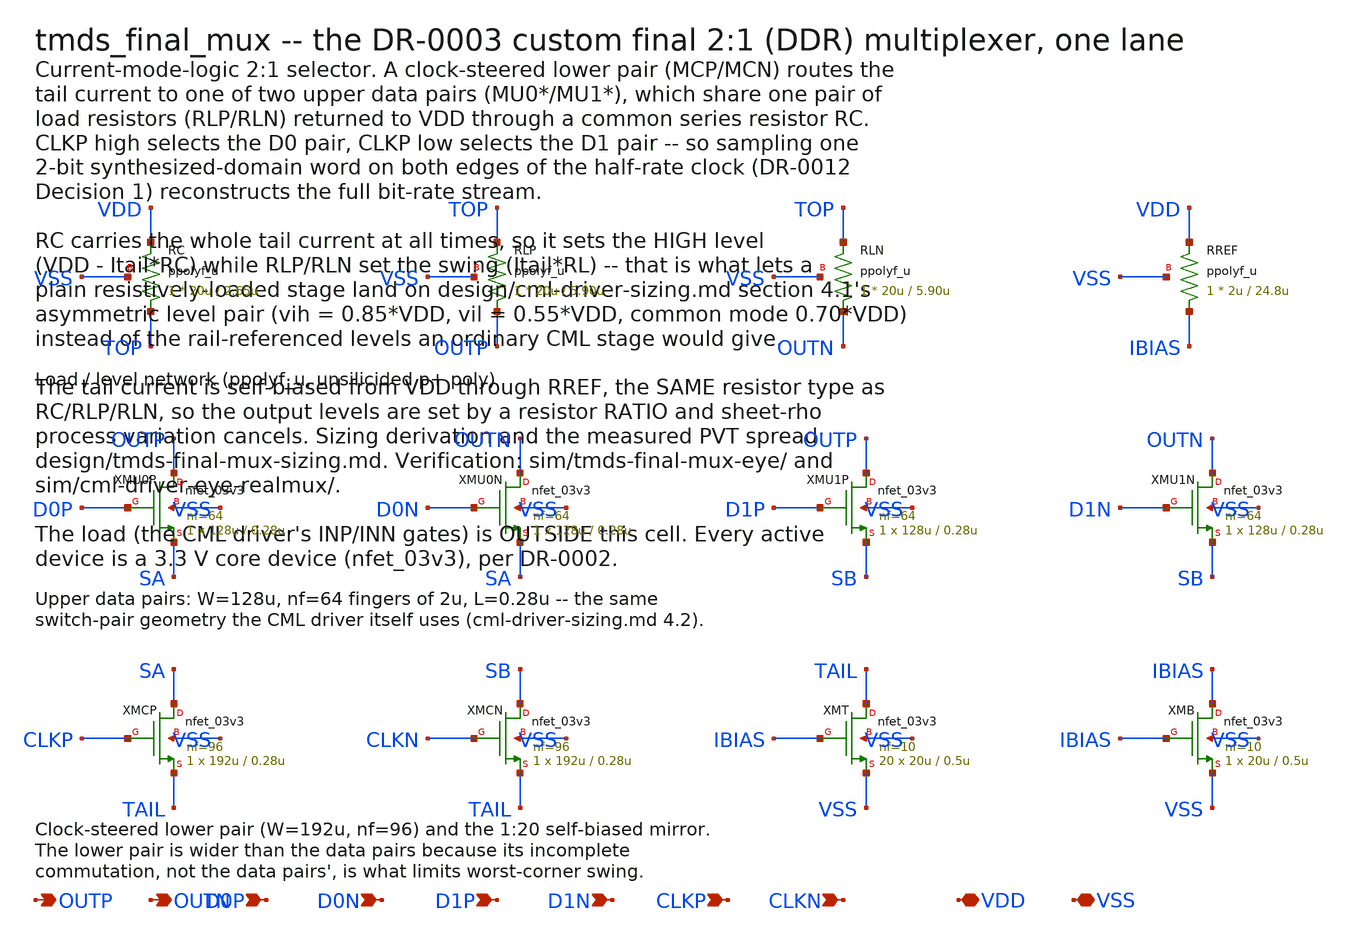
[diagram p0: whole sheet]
** sch_path: design/tmds_final_mux.sch
**.subckt tmds_final_mux OUTP OUTN D0P D0N D1P D1N CLKP CLKN VDD VSS
*.opin OUTP
*.opin OUTN
*.ipin D0P
*.ipin D0N
*.ipin D1P
*.ipin D1N
*.ipin CLKP
*.ipin CLKN
*.iopin VDD
*.iopin VSS
XRC TOP VDD VSS ppolyf_u r_width=20u r_length=2.65u m=1
XRLP OUTP TOP VSS ppolyf_u r_width=20u r_length=5.90u m=1
XRLN OUTN TOP VSS ppolyf_u r_width=20u r_length=5.90u m=1
XRREF IBIAS VDD VSS ppolyf_u r_width=2u r_length=24.8u m=1
XMU0P OUTP D0P SA VSS nfet_03v3 L=0.28u W=128u nf=64 ad=11.52p as=11.88p pd=139.52u ps=143.88u
+ nrd=1.40625m nrs=1.40625m sa=0 sb=0 sd=0 m=1
XMU0N OUTN D0N SA VSS nfet_03v3 L=0.28u W=128u nf=64 ad=11.52p as=11.88p pd=139.52u ps=143.88u
+ nrd=1.40625m nrs=1.40625m sa=0 sb=0 sd=0 m=1
XMU1P OUTP D1P SB VSS nfet_03v3 L=0.28u W=128u nf=64 ad=11.52p as=11.88p pd=139.52u ps=143.88u
+ nrd=1.40625m nrs=1.40625m sa=0 sb=0 sd=0 m=1
XMU1N OUTN D1N SB VSS nfet_03v3 L=0.28u W=128u nf=64 ad=11.52p as=11.88p pd=139.52u ps=143.88u
+ nrd=1.40625m nrs=1.40625m sa=0 sb=0 sd=0 m=1
XMCP SA CLKP TAIL VSS nfet_03v3 L=0.28u W=192u nf=96 ad=17.28p as=17.64p pd=209.28u ps=213.64u
+ nrd=0.9375m nrs=0.9375m sa=0 sb=0 sd=0 m=1
XMCN SB CLKN TAIL VSS nfet_03v3 L=0.28u W=192u nf=96 ad=17.28p as=17.64p pd=209.28u ps=213.64u
+ nrd=0.9375m nrs=0.9375m sa=0 sb=0 sd=0 m=1
XMT TAIL IBIAS VSS VSS nfet_03v3 L=0.5u W=20u nf=10 ad=1.8p as=2.16p pd=21.8u ps=26.16u nrd=9m
+ nrs=9m sa=0 sb=0 sd=0 m=20
XMB IBIAS IBIAS VSS VSS nfet_03v3 L=0.5u W=20u nf=10 ad=1.8p as=2.16p pd=21.8u ps=26.16u nrd=9m
+ nrs=9m sa=0 sb=0 sd=0 m=1
**.ends
.end
